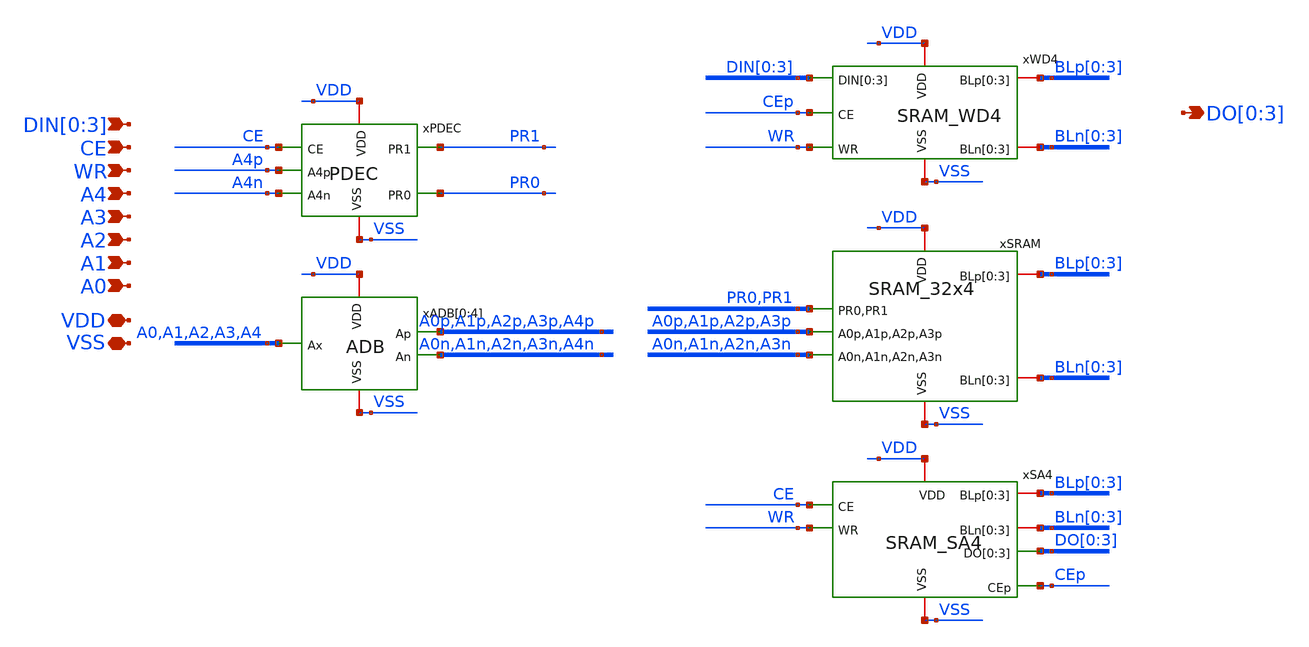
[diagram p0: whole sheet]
** sch_path: module/SRAM128/schematic/SRAM128.sch
**.subckt SRAM128 CE DIN[0],DIN[1],DIN[2],DIN[3] VSS VDD A1 A4 A0 A2 A3 WR DO[0],DO[1],DO[2],DO[3]
*.ipin CE
*.ipin DIN[0],DIN[1],DIN[2],DIN[3]
*.iopin VSS
*.iopin VDD
*.ipin A1
*.ipin A4
*.ipin A0
*.ipin A2
*.ipin A3
*.ipin WR
*.opin DO[0],DO[1],DO[2],DO[3]
xPDEC VDD PR1 CE VSS A4n A4p PR0 PDEC
xADB[0] VDD A0n A0 A0p VSS ADB
xADB[1] VDD A1n A1 A1p VSS ADB
xADB[2] VDD A2n A2 A2p VSS ADB
xADB[3] VDD A3n A3 A3p VSS ADB
xADB[4] VDD A4n A4 A4p VSS ADB
xSRAM PR0 PR1 A0p A1p A2p A3p A0n A1n A2n A3n BLp[0] BLp[1] BLp[2] BLp[3] BLn[0] BLn[1] BLn[2]
+ BLn[3] VDD VSS SRAM_32x4
xSA4 CE WR BLp[0] BLp[1] BLp[2] BLp[3] BLn[0] BLn[1] BLn[2] BLn[3] VDD VSS DO[0] DO[1] DO[2] DO[3]
+ CEp SRAM_SA4
xWD4 DIN[0] DIN[1] DIN[2] DIN[3] CEp WR BLp[0] BLp[1] BLp[2] BLp[3] BLn[0] BLn[1] BLn[2] BLn[3] VDD
+ VSS SRAM_WD4
**.ends
.end
